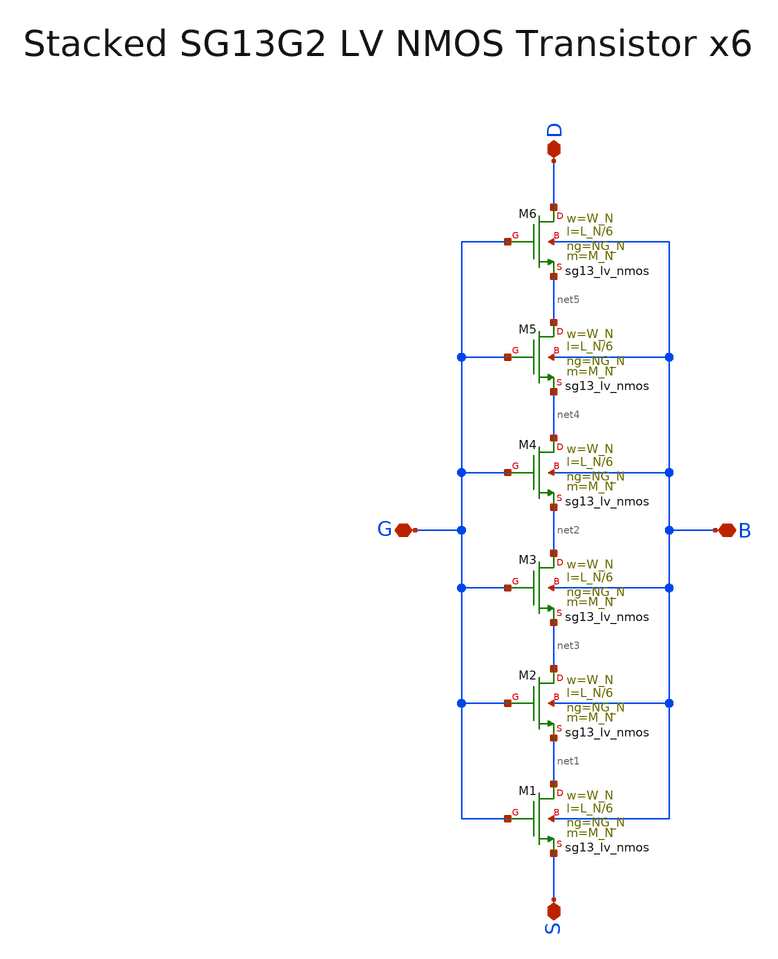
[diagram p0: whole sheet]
** sch_path: SG13G2_ATBS-ADC-main/xschem/stacked_transistors/sg13g2_lv_nmos_stacked/sg13g2_lv_nmos_stacked_x6.sch
**.subckt sg13g2_lv_nmos_stacked_x6 D S G B
*.iopin D
*.iopin S
*.iopin G
*.iopin B
XM1 net1 G S B sg13_lv_nmos w=W_N l=L_N/6 ng=NG_N m=M_N mm_ok=1
XM2 net3 G net1 B sg13_lv_nmos w=W_N l=L_N/6 ng=NG_N m=M_N mm_ok=1
XM3 net2 G net3 B sg13_lv_nmos w=W_N l=L_N/6 ng=NG_N m=M_N mm_ok=1
XM4 net4 G net2 B sg13_lv_nmos w=W_N l=L_N/6 ng=NG_N m=M_N mm_ok=1
XM5 net5 G net4 B sg13_lv_nmos w=W_N l=L_N/6 ng=NG_N m=M_N mm_ok=1
XM6 D G net5 B sg13_lv_nmos w=W_N l=L_N/6 ng=NG_N m=M_N mm_ok=1
**.ends
.end
